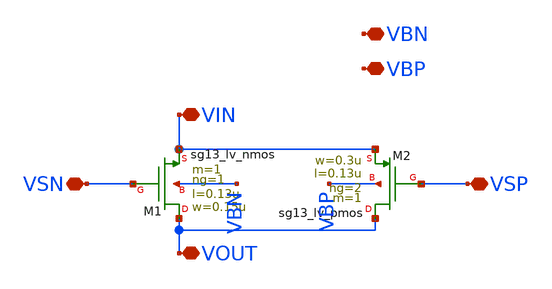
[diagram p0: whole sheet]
** sch_path: CDR4176-main/schematic/xschem/tg_custom/tg_custom.sch
**.subckt tg_custom VIN VSN VOUT VSP VBN VBP
*.iopin VIN
*.iopin VSN
*.iopin VOUT
*.iopin VSP
*.iopin VBN
*.iopin VBP
XM1 VOUT VSN VIN VBN sg13_lv_nmos w=0.15u l=0.13u ng=1 m=1 mm_ok=1
XM2 VOUT VSP VIN VBP sg13_lv_pmos w=0.3u l=0.13u ng=2 m=1 mm_ok=1
**.ends
.end
